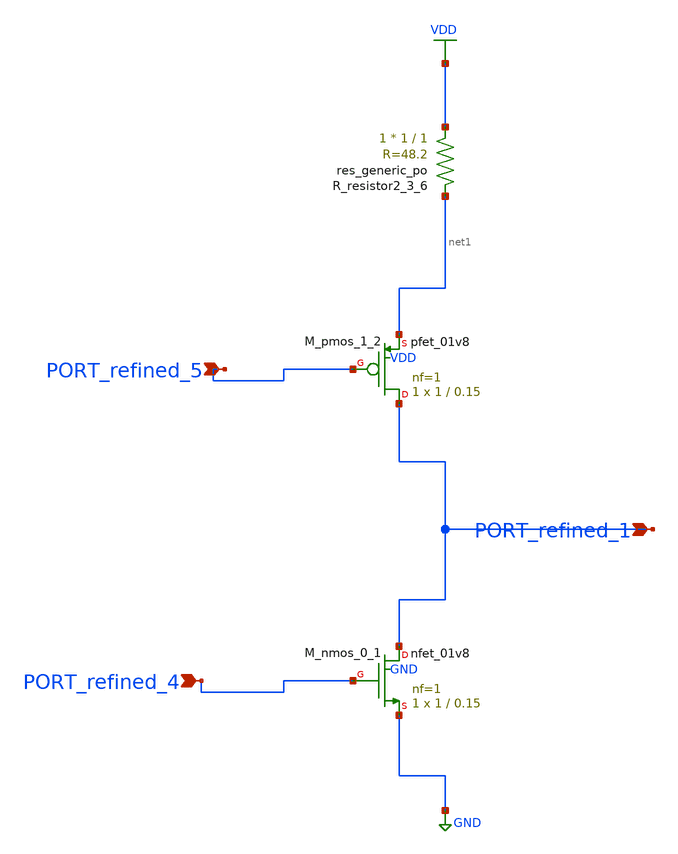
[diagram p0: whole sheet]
** sch_path: schematics/AMSNet/529.sch
**.subckt 529 PORT_refined_5 PORT_refined_1 PORT_refined_4
*.ipin PORT_refined_5
*.ipin PORT_refined_1
*.ipin PORT_refined_4
XM_nmos_0_1 PORT_refined_1 PORT_refined_4 GND GND sky130_fd_pr__nfet_01v8 L=0.15 W=1 nf=1 ad='int((1 + 1)/2) * 1 / 1 * 0.29'
+ as='int((1 + 2)/2) * 1 / 1 * 0.29' pd='2*int((1 + 1)/2) * (1 / 1 + 0.29)' ps='2*int((1 + 2)/2) * (1 / 1 + 0.29)'
+ nrd='0.29 / 1 ' nrs='0.29 / 1 ' sa=0 sb=0 sd=0 mult=1 m=1
XM_pmos_1_2 PORT_refined_1 PORT_refined_5 net1 VDD sky130_fd_pr__pfet_01v8 L=0.15 W=1 nf=1 ad='int((1 + 1)/2) * 1 / 1 * 0.29'
+ as='int((1 + 2)/2) * 1 / 1 * 0.29' pd='2*int((1 + 1)/2) * (1 / 1 + 0.29)' ps='2*int((1 + 2)/2) * (1 / 1 + 0.29)'
+ nrd='0.29 / 1 ' nrs='0.29 / 1 ' sa=0 sb=0 sd=0 mult=1 m=1
XR_resistor2_3_6 VDD net1 sky130_fd_pr__res_generic_po W=1 L=1 m=1
**.ends
.GLOBAL GND
.GLOBAL VDD
.end
